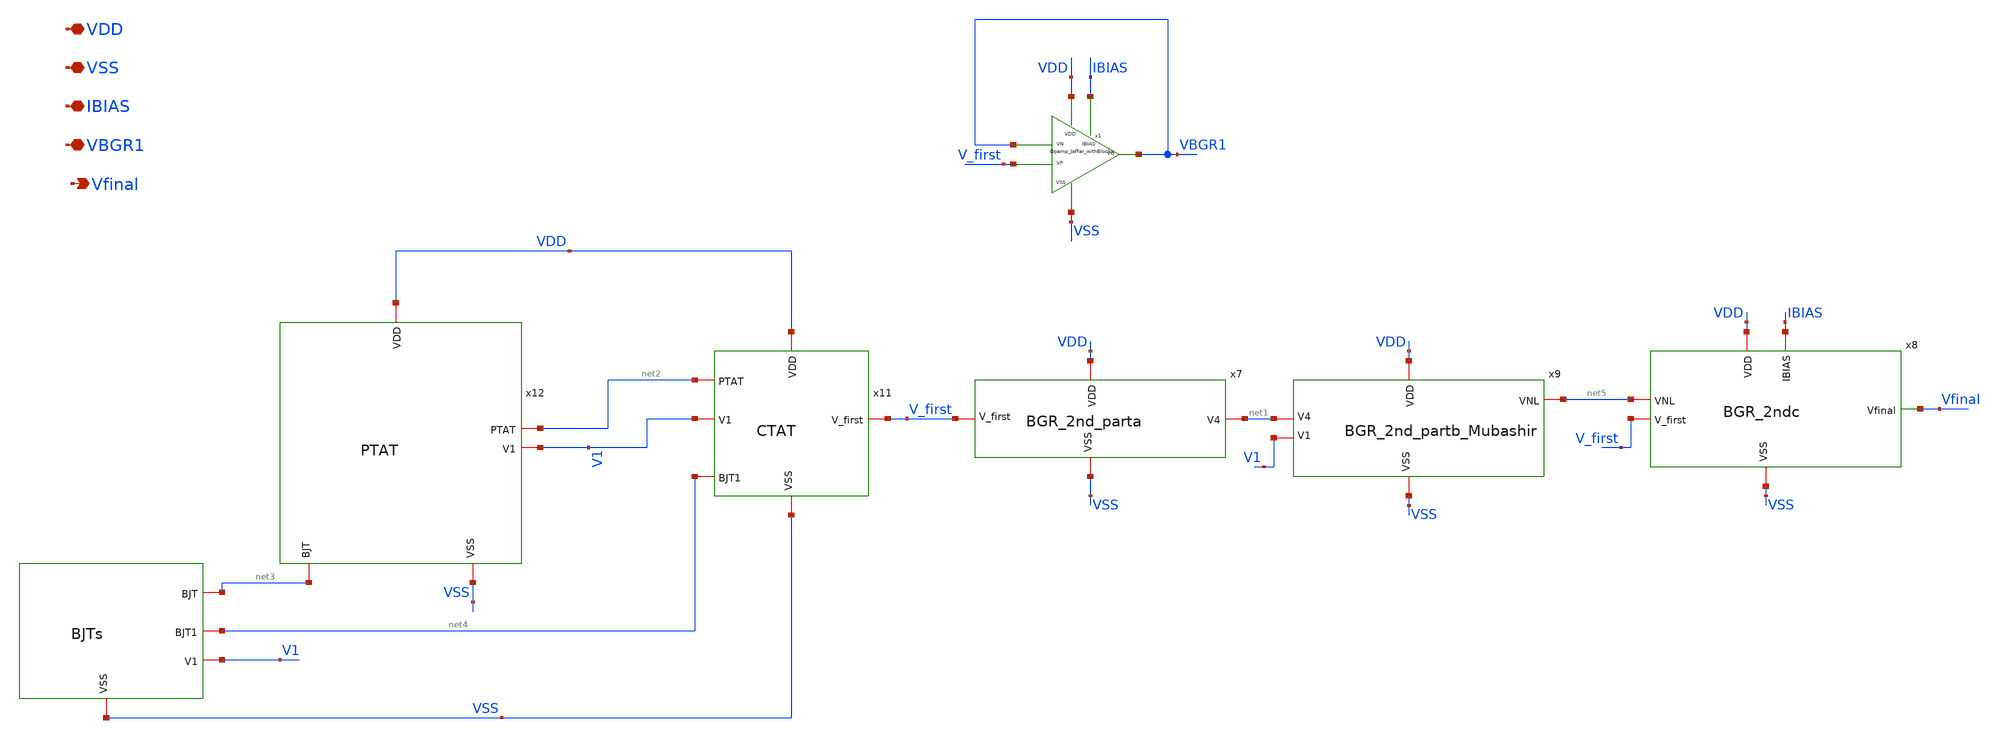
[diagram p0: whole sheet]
** sch_path: xschem/xschem_BGR_Top/BGR_Toplevel_Testing.sch
**.subckt BGR_Toplevel_Testing Vfinal VDD VSS VBGR1 IBIAS
*.opin Vfinal
*.iopin VDD
*.iopin VSS
*.iopin VBGR1
*.iopin IBIAS
x7 VDD VSS V_first net1 BGR_2nd_parta
x8 VDD VSS net5 V_first IBIAS Vfinal BGR_2ndc
x9 VDD VSS V1 net1 net5 BGR_2nd_partb_Mubashir
x10 net3 VSS net4 V1 BJTs
x11 VDD net2 V1 V_first VSS net4 CTAT
x12 VDD net2 V1 net3 VSS PTAT
x1 VDD VSS V_first VBGR1 VBGR1 IBIAS Opamp_Jaffar_withBlocks
**.ends
.end
